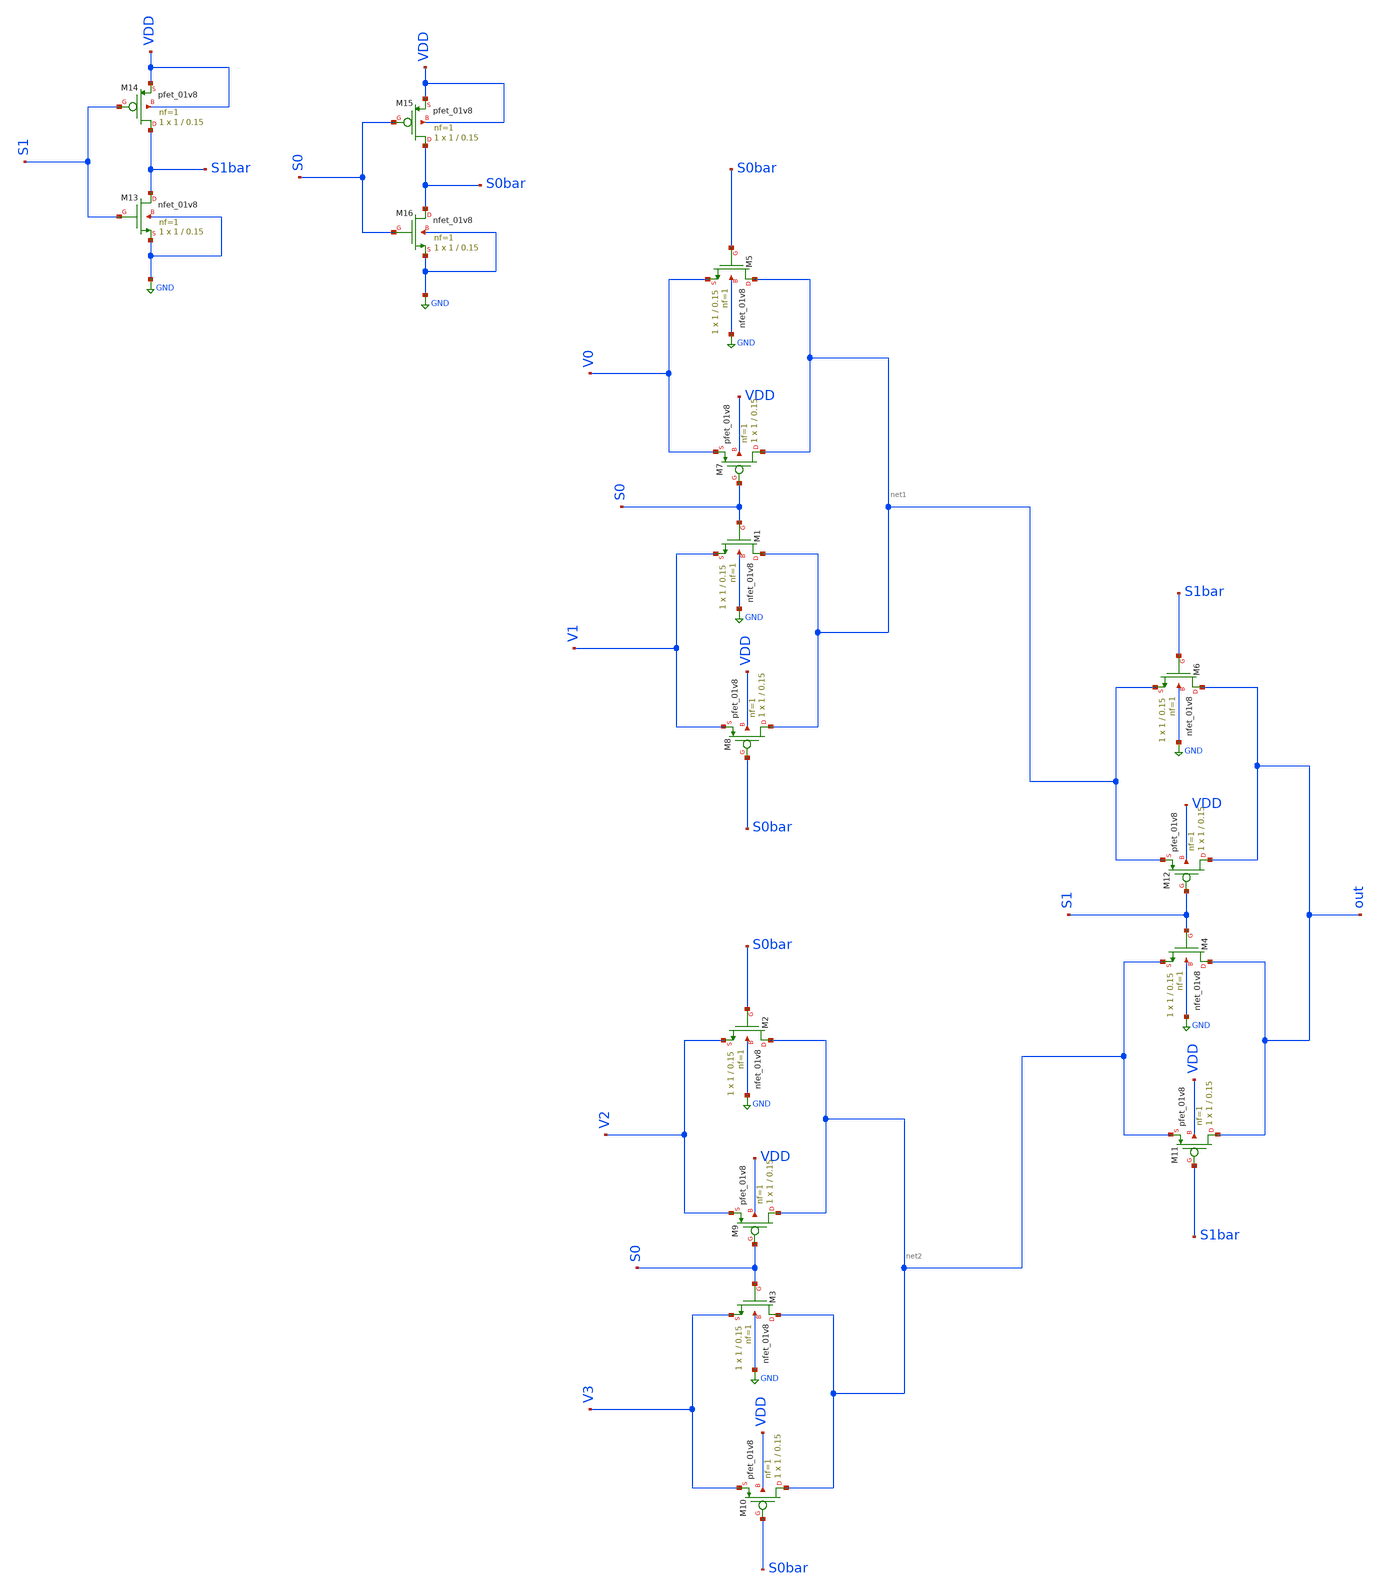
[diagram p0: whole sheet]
** sch_path: mag/mux_inv_xschem.sch
**.subckt mux_inv_xschem
XM5 net1 S0bar V0 GND sky130_fd_pr__nfet_01v8 L=0.15 W=1 nf=1 ad='int((nf+1)/2) * W/nf * 0.29' as='int((nf+2)/2) * W/nf * 0.29'
+ pd='2*int((nf+1)/2) * (W/nf + 0.29)' ps='2*int((nf+2)/2) * (W/nf + 0.29)' nrd='0.29 / W' nrs='0.29 / W'
+ sa=0 sb=0 sd=0 mult=1 m=1
XM1 net1 S0 V1 GND sky130_fd_pr__nfet_01v8 L=0.15 W=1 nf=1 ad='int((nf+1)/2) * W/nf * 0.29' as='int((nf+2)/2) * W/nf * 0.29'
+ pd='2*int((nf+1)/2) * (W/nf + 0.29)' ps='2*int((nf+2)/2) * (W/nf + 0.29)' nrd='0.29 / W' nrs='0.29 / W'
+ sa=0 sb=0 sd=0 mult=1 m=1
XM2 net2 S0bar V2 GND sky130_fd_pr__nfet_01v8 L=0.15 W=1 nf=1 ad='int((nf+1)/2) * W/nf * 0.29' as='int((nf+2)/2) * W/nf * 0.29'
+ pd='2*int((nf+1)/2) * (W/nf + 0.29)' ps='2*int((nf+2)/2) * (W/nf + 0.29)' nrd='0.29 / W' nrs='0.29 / W'
+ sa=0 sb=0 sd=0 mult=1 m=1
XM3 net2 S0 V3 GND sky130_fd_pr__nfet_01v8 L=0.15 W=1 nf=1 ad='int((nf+1)/2) * W/nf * 0.29' as='int((nf+2)/2) * W/nf * 0.29'
+ pd='2*int((nf+1)/2) * (W/nf + 0.29)' ps='2*int((nf+2)/2) * (W/nf + 0.29)' nrd='0.29 / W' nrs='0.29 / W'
+ sa=0 sb=0 sd=0 mult=1 m=1
XM4 out S1 net2 GND sky130_fd_pr__nfet_01v8 L=0.15 W=1 nf=1 ad='int((nf+1)/2) * W/nf * 0.29' as='int((nf+2)/2) * W/nf * 0.29'
+ pd='2*int((nf+1)/2) * (W/nf + 0.29)' ps='2*int((nf+2)/2) * (W/nf + 0.29)' nrd='0.29 / W' nrs='0.29 / W'
+ sa=0 sb=0 sd=0 mult=1 m=1
XM6 out S1bar net1 GND sky130_fd_pr__nfet_01v8 L=0.15 W=1 nf=1 ad='int((nf+1)/2) * W/nf * 0.29' as='int((nf+2)/2) * W/nf * 0.29'
+ pd='2*int((nf+1)/2) * (W/nf + 0.29)' ps='2*int((nf+2)/2) * (W/nf + 0.29)' nrd='0.29 / W' nrs='0.29 / W'
+ sa=0 sb=0 sd=0 mult=1 m=1
XM7 net1 S0 V0 VDD sky130_fd_pr__pfet_01v8 L=0.15 W=1 nf=1 ad='int((nf+1)/2) * W/nf * 0.29' as='int((nf+2)/2) * W/nf * 0.29'
+ pd='2*int((nf+1)/2) * (W/nf + 0.29)' ps='2*int((nf+2)/2) * (W/nf + 0.29)' nrd='0.29 / W' nrs='0.29 / W'
+ sa=0 sb=0 sd=0 mult=1 m=1
XM8 net1 S0bar V1 VDD sky130_fd_pr__pfet_01v8 L=0.15 W=1 nf=1 ad='int((nf+1)/2) * W/nf * 0.29' as='int((nf+2)/2) * W/nf * 0.29'
+ pd='2*int((nf+1)/2) * (W/nf + 0.29)' ps='2*int((nf+2)/2) * (W/nf + 0.29)' nrd='0.29 / W' nrs='0.29 / W'
+ sa=0 sb=0 sd=0 mult=1 m=1
XM9 net2 S0 V2 VDD sky130_fd_pr__pfet_01v8 L=0.15 W=1 nf=1 ad='int((nf+1)/2) * W/nf * 0.29' as='int((nf+2)/2) * W/nf * 0.29'
+ pd='2*int((nf+1)/2) * (W/nf + 0.29)' ps='2*int((nf+2)/2) * (W/nf + 0.29)' nrd='0.29 / W' nrs='0.29 / W'
+ sa=0 sb=0 sd=0 mult=1 m=1
XM10 net2 S0bar V3 VDD sky130_fd_pr__pfet_01v8 L=0.15 W=1 nf=1 ad='int((nf+1)/2) * W/nf * 0.29' as='int((nf+2)/2) * W/nf * 0.29'
+ pd='2*int((nf+1)/2) * (W/nf + 0.29)' ps='2*int((nf+2)/2) * (W/nf + 0.29)' nrd='0.29 / W' nrs='0.29 / W'
+ sa=0 sb=0 sd=0 mult=1 m=1
XM11 out S1bar net2 VDD sky130_fd_pr__pfet_01v8 L=0.15 W=1 nf=1 ad='int((nf+1)/2) * W/nf * 0.29' as='int((nf+2)/2) * W/nf * 0.29'
+ pd='2*int((nf+1)/2) * (W/nf + 0.29)' ps='2*int((nf+2)/2) * (W/nf + 0.29)' nrd='0.29 / W' nrs='0.29 / W'
+ sa=0 sb=0 sd=0 mult=1 m=1
XM12 out S1 net1 VDD sky130_fd_pr__pfet_01v8 L=0.15 W=1 nf=1 ad='int((nf+1)/2) * W/nf * 0.29' as='int((nf+2)/2) * W/nf * 0.29'
+ pd='2*int((nf+1)/2) * (W/nf + 0.29)' ps='2*int((nf+2)/2) * (W/nf + 0.29)' nrd='0.29 / W' nrs='0.29 / W'
+ sa=0 sb=0 sd=0 mult=1 m=1
XM13 S1bar S1 GND GND sky130_fd_pr__nfet_01v8 L=0.15 W=1 nf=1 ad='int((nf+1)/2) * W/nf * 0.29' as='int((nf+2)/2) * W/nf * 0.29'
+ pd='2*int((nf+1)/2) * (W/nf + 0.29)' ps='2*int((nf+2)/2) * (W/nf + 0.29)' nrd='0.29 / W' nrs='0.29 / W'
+ sa=0 sb=0 sd=0 mult=1 m=1
XM14 S1bar S1 VDD VDD sky130_fd_pr__pfet_01v8 L=0.15 W=1 nf=1 ad='int((nf+1)/2) * W/nf * 0.29' as='int((nf+2)/2) * W/nf * 0.29'
+ pd='2*int((nf+1)/2) * (W/nf + 0.29)' ps='2*int((nf+2)/2) * (W/nf + 0.29)' nrd='0.29 / W' nrs='0.29 / W'
+ sa=0 sb=0 sd=0 mult=1 m=1
XM15 S0bar S0 VDD VDD sky130_fd_pr__pfet_01v8 L=0.15 W=1 nf=1 ad='int((nf+1)/2) * W/nf * 0.29' as='int((nf+2)/2) * W/nf * 0.29'
+ pd='2*int((nf+1)/2) * (W/nf + 0.29)' ps='2*int((nf+2)/2) * (W/nf + 0.29)' nrd='0.29 / W' nrs='0.29 / W'
+ sa=0 sb=0 sd=0 mult=1 m=1
XM16 S0bar S0 GND GND sky130_fd_pr__nfet_01v8 L=0.15 W=1 nf=1 ad='int((nf+1)/2) * W/nf * 0.29' as='int((nf+2)/2) * W/nf * 0.29'
+ pd='2*int((nf+1)/2) * (W/nf + 0.29)' ps='2*int((nf+2)/2) * (W/nf + 0.29)' nrd='0.29 / W' nrs='0.29 / W'
+ sa=0 sb=0 sd=0 mult=1 m=1
**.ends
.GLOBAL GND
.end
